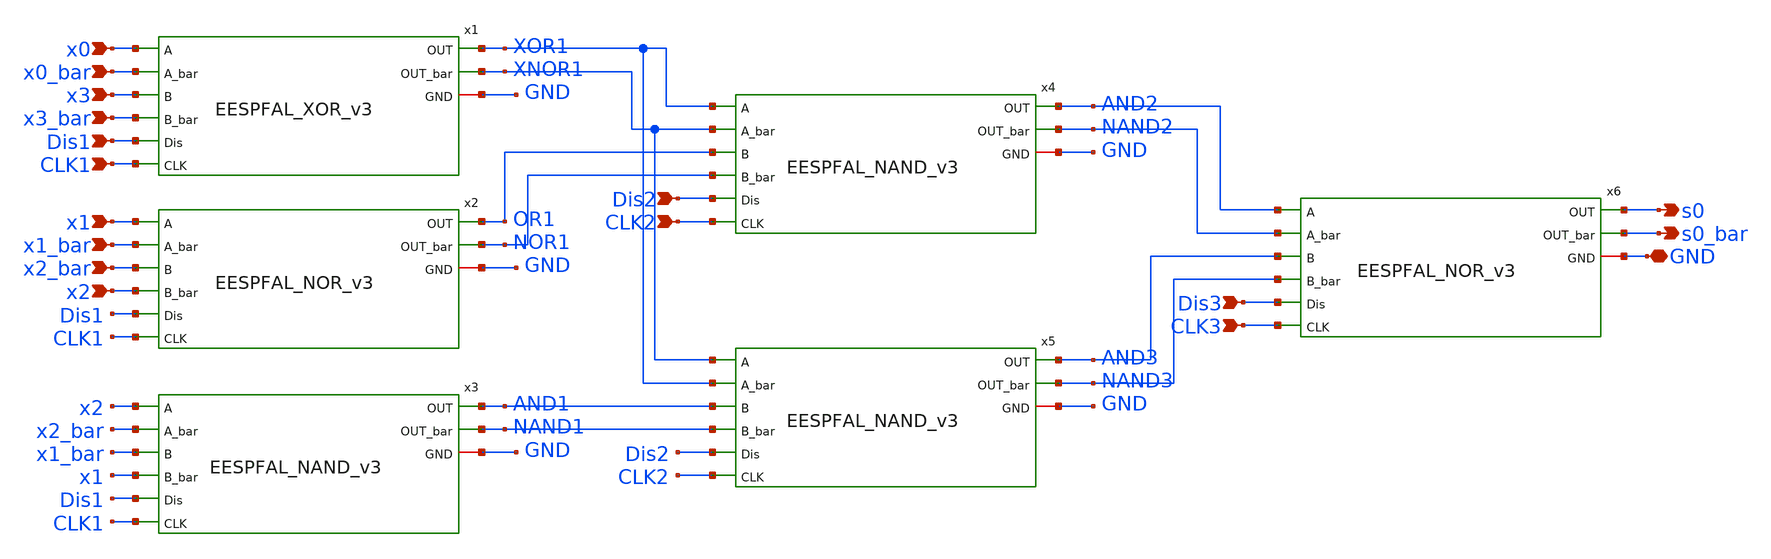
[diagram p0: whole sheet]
** sch_path: skywater_stuff/EESPFAL_s0_magic_checked.sch
**.subckt EESPFAL_s0_magic_checked x0 x0_bar x1 x1_bar x2 x2_bar x3 x3_bar s0 s0_bar Dis1 Dis2 Dis3
*+ GND CLK1 CLK2 CLK3
*.ipin x0
*.ipin x0_bar
*.ipin x1
*.ipin x1_bar
*.ipin x2
*.ipin x2_bar
*.ipin x3
*.ipin x3_bar
*.opin s0
*.opin s0_bar
*.ipin Dis1
*.ipin Dis2
*.ipin Dis3
*.iopin GND
*.ipin CLK1
*.ipin CLK2
*.ipin CLK3
x1 x0 x0_bar x3 x3_bar XOR1 XNOR1 Dis1 GND CLK1 EESPFAL_XOR_v3
x4 XOR1 XNOR1 OR1 NOR1 AND2 NAND2 Dis2 GND CLK2 EESPFAL_NAND_v3
x5 XNOR1 XOR1 AND1 NAND1 AND3 NAND3 Dis2 GND CLK2 EESPFAL_NAND_v3
x6 AND2 NAND2 AND3 NAND3 s0 s0_bar Dis3 GND CLK3 EESPFAL_NOR_v3
x2 x1 x1_bar x2_bar x2 OR1 NOR1 Dis1 GND CLK1 EESPFAL_NOR_v3
x3 x2 x2_bar x1_bar x1 AND1 NAND1 Dis1 GND CLK1 EESPFAL_NAND_v3
**.ends
.end
